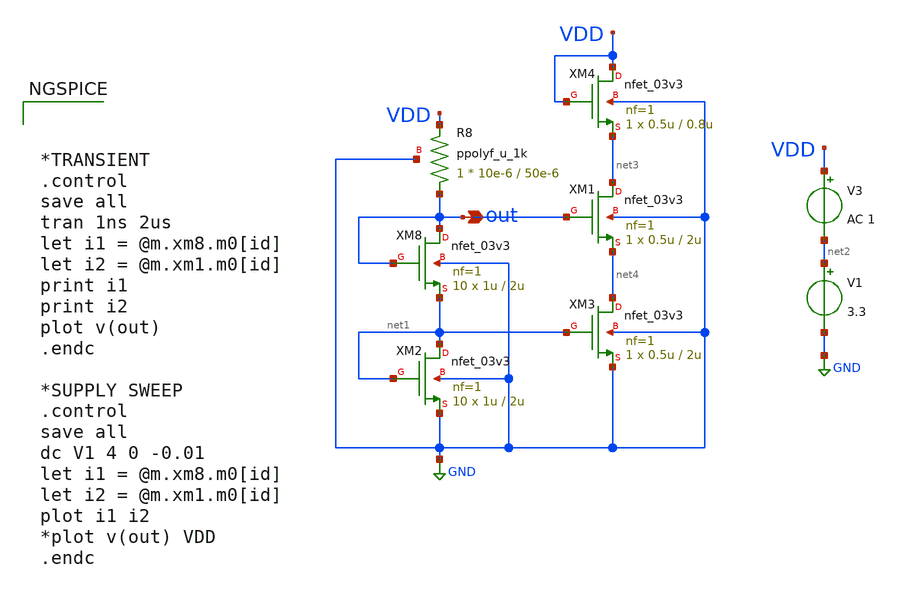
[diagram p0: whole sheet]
** sch_path: LDO/xschem/isource/isource.sch

.include $env(PDK_ROOT)/$env(PDK)/libs.tech/ngspice/design.ngspice
.lib $env(PDK_ROOT)/$env(PDK)/libs.tech/ngspice/sm141064.ngspice typical
.lib $env(PDK_ROOT)/$env(PDK)/libs.tech/ngspice/sm141064.ngspice mimcap_statistical
.lib $env(PDK_ROOT)/$env(PDK)/libs.tech/ngspice/sm141064.ngspice cap_mim
.lib $env(PDK_ROOT)/$env(PDK)/libs.tech/ngspice/sm141064.ngspice res_typical
.lib $env(PDK_ROOT)/$env(PDK)/libs.tech/ngspice/sm141064.ngspice bjt_typical
.lib $env(PDK_ROOT)/$env(PDK)/libs.tech/ngspice/sm141064.ngspice moscap_typical

**.subckt isource out
*.opin out
XM8 out out net1 GND nfet_03v3 L=2u W=1u nf=1 ad='int((nf+1)/2) * W/nf * 0.18u' as='int((nf+2)/2) * W/nf * 0.18u'
+ pd='2*int((nf+1)/2) * (W/nf + 0.18u)' ps='2*int((nf+2)/2) * (W/nf + 0.18u)' nrd='0.18u / W' nrs='0.18u / W'
+ sa=0 sb=0 sd=0 m=10
XR8 out VDD GND ppolyf_u_1k r_width=10e-6 r_length=50e-6 m=1
V1 net2 GND 3.3
V3 VDD net2 AC 1
XM1 net3 out net4 GND nfet_03v3 L=2u W=0.5u nf=1 ad='int((nf+1)/2) * W/nf * 0.18u' as='int((nf+2)/2) * W/nf * 0.18u'
+ pd='2*int((nf+1)/2) * (W/nf + 0.18u)' ps='2*int((nf+2)/2) * (W/nf + 0.18u)' nrd='0.18u / W' nrs='0.18u / W'
+ sa=0 sb=0 sd=0 m=1
XM2 net1 net1 GND GND nfet_03v3 L=2u W=1u nf=1 ad='int((nf+1)/2) * W/nf * 0.18u' as='int((nf+2)/2) * W/nf * 0.18u'
+ pd='2*int((nf+1)/2) * (W/nf + 0.18u)' ps='2*int((nf+2)/2) * (W/nf + 0.18u)' nrd='0.18u / W' nrs='0.18u / W'
+ sa=0 sb=0 sd=0 m=10
XM3 net4 net1 GND GND nfet_03v3 L=2u W=0.5u nf=1 ad='int((nf+1)/2) * W/nf * 0.18u' as='int((nf+2)/2) * W/nf * 0.18u'
+ pd='2*int((nf+1)/2) * (W/nf + 0.18u)' ps='2*int((nf+2)/2) * (W/nf + 0.18u)' nrd='0.18u / W' nrs='0.18u / W'
+ sa=0 sb=0 sd=0 m=1
XM4 VDD VDD net3 GND nfet_03v3 L=0.8u W=0.5u nf=1 ad='int((nf+1)/2) * W/nf * 0.18u' as='int((nf+2)/2) * W/nf * 0.18u'
+ pd='2*int((nf+1)/2) * (W/nf + 0.18u)' ps='2*int((nf+2)/2) * (W/nf + 0.18u)' nrd='0.18u / W' nrs='0.18u / W'
+ sa=0 sb=0 sd=0 m=1
**** begin user architecture code



*TRANSIENT
.control
save all
tran 1ns 2us
let i1 = @m.xm8.m0[id]
let i2 = @m.xm1.m0[id]
print i1
print i2
plot v(out)
.endc

*SUPPLY SWEEP
.control
save all
dc V1 4 0 -0.01
let i1 = @m.xm8.m0[id]
let i2 = @m.xm1.m0[id]
plot i1 i2
*plot v(out) VDD
.endc



**** end user architecture code
**.ends
.GLOBAL GND
.end
